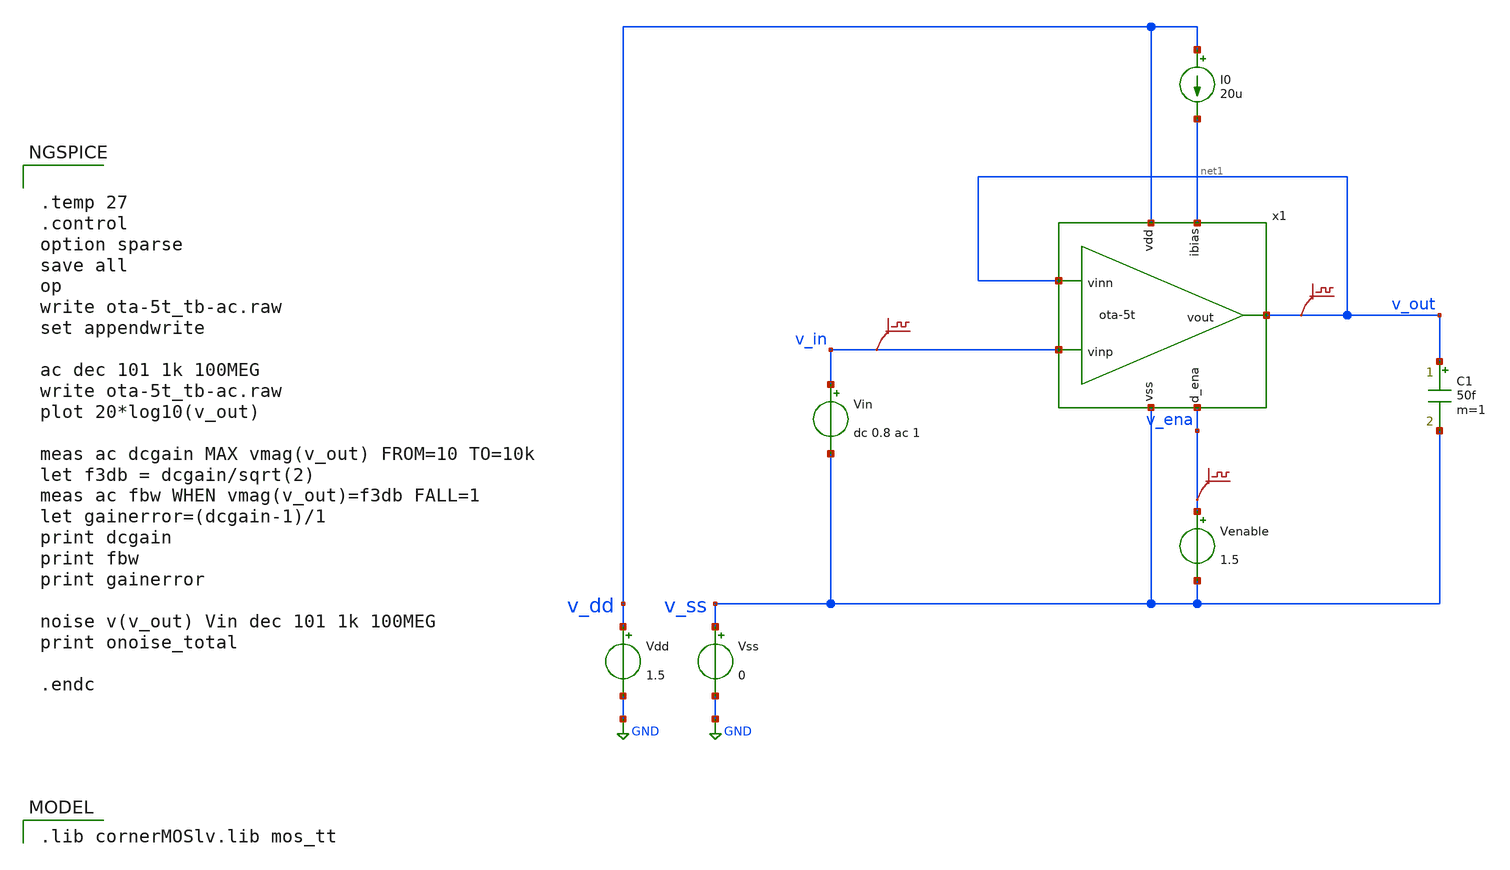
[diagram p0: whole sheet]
** sch_path: prj/template/3_Real_circuits/ota-5t_tb-ac.sch
* (c) 2024-2025 H. Pretl, Apache-2.0 license
**.subckt ota-5t_tb-ac
Vdd v_dd GND 1.5
Vss v_ss GND 0
C1 v_out v_ss 50f m=1
Vin v_in v_ss dc 0.8 ac 1
I0 v_dd net1 20u
Venable v_ena v_ss 1.5
.save v(v_in)
.save v(v_out)
.save v(v_ena)
x1 v_dd v_out v_out v_in net1 v_ena v_ss ota-5t
**** begin user architecture code
 .lib cornerMOSlv.lib mos_tt



.temp 27
.control
option sparse
save all
op
write ota-5t_tb-ac.raw
set appendwrite

ac dec 101 1k 100MEG
write ota-5t_tb-ac.raw
plot 20*log10(v_out)

meas ac dcgain MAX vmag(v_out) FROM=10 TO=10k
let f3db = dcgain/sqrt(2)
meas ac fbw WHEN vmag(v_out)=f3db FALL=1
let gainerror=(dcgain-1)/1
print dcgain
print fbw
print gainerror

noise v(v_out) Vin dec 101 1k 100MEG
print onoise_total

.endc


**** end user architecture code
**.ends

* expanding   symbol:  ota-5t.sym # of pins=7
** sym_path: prj/template/3_Real_circuits/ota-5t.sym
** sch_path: prj/template/3_Real_circuits/ota-5t.sch
.subckt ota-5t vdd vout vinn vinp ibias d_ena vss
*.ipin ibias
*.iopin vdd
*.iopin vss
*.ipin vinp
*.ipin vinn
*.opin vout
*.ipin d_ena
XM5 tail gate_n vss vss sg13_lv_nmos w=0.5u l=5u ng=1 m=1 mm_ok=1
XM4 vout gate_p vdd vdd sg13_lv_pmos w=1.5u l=5u ng=1 m=1 mm_ok=1
XM1 gate_p vinp tail vss sg13_lv_nmos w=2u l=5u ng=1 m=1 mm_ok=1
XM2 vout vinn tail vss sg13_lv_nmos w=2u l=5u ng=1 m=1 mm_ok=1
XM3 gate_p gate_p vdd vdd sg13_lv_pmos w=1.5u l=5u ng=1 m=1 mm_ok=1
XM6 ibias gate_n vss vss sg13_lv_nmos w=2.5u l=5u ng=5 m=1 mm_ok=1
XM9 gate_n ena_n vss vss sg13_lv_nmos w=0.5u l=0.13u ng=1 m=1 mm_ok=1
XM11 gate_p ena vdd vdd sg13_lv_pmos w=1.5u l=0.13u ng=1 m=1 mm_ok=1
XM7 ena ena_n vss vss sg13_lv_nmos w=0.5u l=0.13u ng=1 m=1 mm_ok=1
XM8 ena ena_n vdd vdd sg13_lv_pmos w=1.5u l=0.13u ng=1 m=1 mm_ok=1
XM10 ibias ena gate_n vss sg13_lv_nmos w=0.5u l=0.13u ng=1 m=1 mm_ok=1
XM12 ena_n d_ena vss vss sg13_lv_nmos w=0.5u l=0.13u ng=1 m=1 mm_ok=1
XM13 ena_n d_ena vdd vdd sg13_lv_pmos w=1.5u l=0.13u ng=1 m=1 mm_ok=1
.ends

.GLOBAL GND
.end
